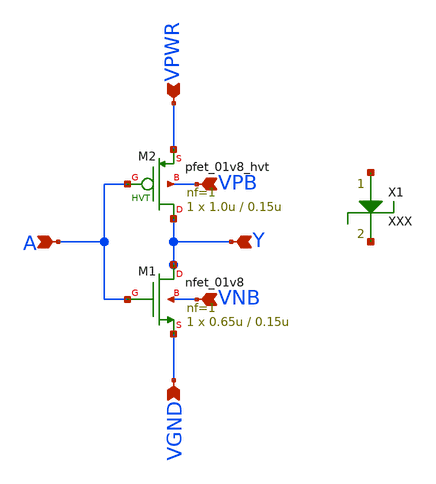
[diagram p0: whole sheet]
** sch_path: LVS_Resources/inverter.sch
**.subckt inverter A VGND VNB VPB VPWR Y
*.ipin A
*.ipin VGND
*.ipin VNB
*.ipin VPB
*.ipin VPWR
*.ipin Y
MM1 Y A VGND VNB sky130_fd_pr__nfet_01v8 L=0.15u W=0.65u nf=1 ad='int((1 + 1)/2) * 0.65u / 1 * 0.29'
+ as='int((1 + 2)/2) * 0.65u / 1 * 0.29' pd='2*int((1 + 1)/2) * (0.65u / 1 + 0.29)' ps='2*int((1 + 2)/2) * (0.65u / 1 + 0.29)'
+ nrd='0.29 / 0.65u ' nrs='0.29 / 0.65u ' sa=0 sb=0 sd=0 mult=1 m=1
MM2 Y A VPWR VPB sky130_fd_pr__pfet_01v8_hvt L=0.15u W=1.0u nf=1 ad='int((1 + 1)/2) * 1.0u / 1 * 0.29'
+ as='int((1 + 2)/2) * 1.0u / 1 * 0.29' pd='2*int((1 + 1)/2) * (1.0u / 1 + 0.29)' ps='2*int((1 + 2)/2) * (1.0u / 1 + 0.29)'
+ nrd='0.29 / 1.0u ' nrs='0.29 / 1.0u ' sa=0 sb=0 sd=0 mult=1 m=1
X1 net1 net2 XXX
**.ends
.end
